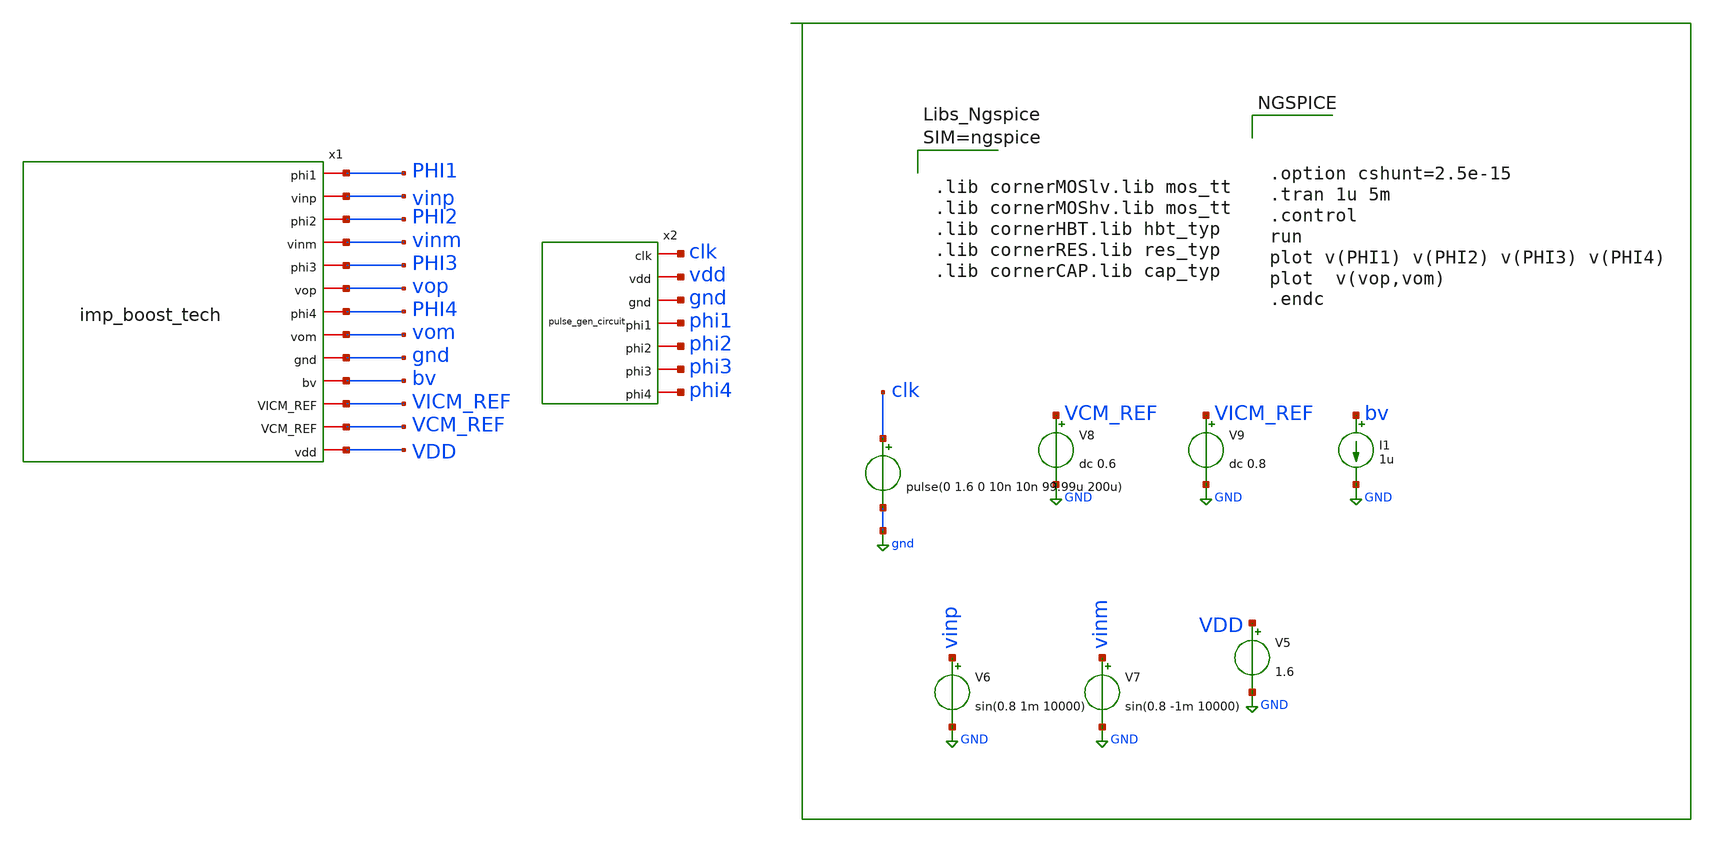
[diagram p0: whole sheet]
** sch_path: dependencies/OTA/OTA-main/schematic/xschem/digital_pulse_ina.sch
**.subckt digital_pulse_ina
V5 VDD GND 1.6
V8 VCM_REF GND dc 0.6
V9 VICM_REF GND dc 0.8
I1 bv GND 1u
x1 PHI1 vinp PHI2 vinm PHI3 vop PHI4 vom gnd bv VICM_REF VCM_REF VDD imp_boost_tech
V6 vinp GND sin(0.8 1m 10000)
V7 vinm GND sin(0.8 -1m 10000)
x2 clk vdd gnd phi1 phi2 phi3 phi4 pulse_gen_circuit
V1 clk gnd pulse(0 1.6 0 10n 10n 99.99u 200u)
**** begin user architecture code



.lib cornerMOSlv.lib mos_tt
.lib cornerMOShv.lib mos_tt
.lib cornerHBT.lib hbt_typ
.lib cornerRES.lib res_typ
.lib cornerCAP.lib cap_typ






.option cshunt=2.5e-15
.tran 1u 5m
.control
run
plot v(PHI1) v(PHI2) v(PHI3) v(PHI4)
plot  v(vop,vom)
.endc



**** end user architecture code
**.ends
.GLOBAL GND
.GLOBAL gnd
.end
